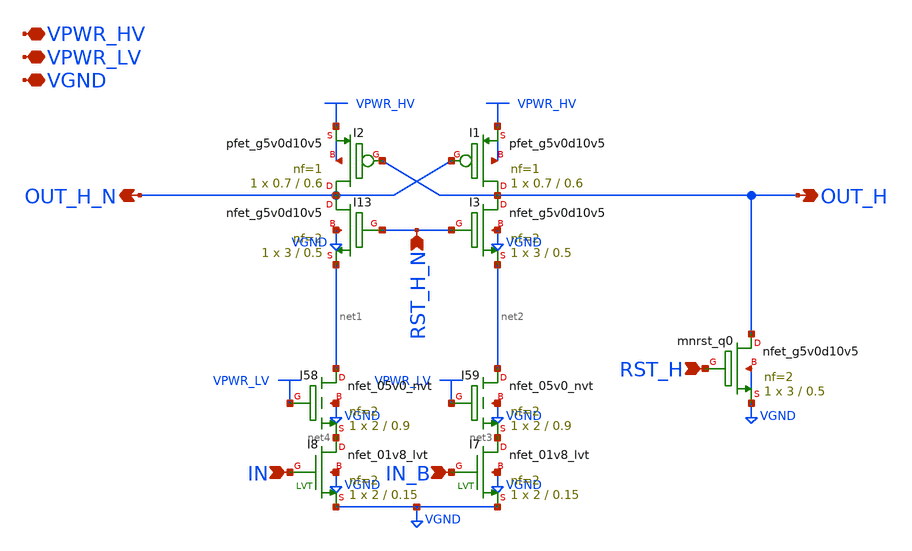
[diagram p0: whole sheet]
** sch_path: gpiov2_amux_drvr_ls.sch
* Copyright 2023 David Mitchell Bailey
* Licensed under the Apache License, Version 2.0 (the "License");
* you may not use this file except in compliance with the License.
* You may obtain a copy of the License at
* https://www.apache.org/licenses/LICENSE-2.0
* Unless required by applicable law or agreed to in writing, software
* distributed under the License is distributed on an "AS IS" BASIS,
* WITHOUT WARRANTIES OR CONDITIONS OF ANY KIND, either express or implied.
* See the License for the specific language governing permissions and
* limitations under the License.
**.subckt gpiov2_amux_drvr_ls RST_H OUT_H VPWR_LV VGND OUT_H_N RST_H_N IN IN_B VPWR_HV
*.ipin RST_H
*.opin OUT_H
*.iopin VPWR_LV
*.iopin VGND
*.opin OUT_H_N
*.ipin RST_H_N
*.ipin IN
*.ipin IN_B
*.iopin VPWR_HV
XI13 OUT_H_N RST_H_N net1 VGND sky130_fd_pr__nfet_g5v0d10v5 L=0.5 W=3 nf=2 ad='int((nf+1)/2) * W/nf * 0.29'
+ as='int((nf+2)/2) * W/nf * 0.29' pd='2*int((nf+1)/2) * (W/nf + 0.29)' ps='2*int((nf+2)/2) * (W/nf + 0.29)'
+ nrd='0.29 / W' nrs='0.29 / W' sa=0 sb=0 sd=0 mult=1 m=1
XI3 OUT_H RST_H_N net2 VGND sky130_fd_pr__nfet_g5v0d10v5 L=0.5 W=3 nf=2 ad='int((nf+1)/2) * W/nf * 0.29'
+ as='int((nf+2)/2) * W/nf * 0.29' pd='2*int((nf+1)/2) * (W/nf + 0.29)' ps='2*int((nf+2)/2) * (W/nf + 0.29)'
+ nrd='0.29 / W' nrs='0.29 / W' sa=0 sb=0 sd=0 mult=1 m=1
XI1 OUT_H OUT_H_N VPWR_HV VPWR_HV sky130_fd_pr__pfet_g5v0d10v5 L=0.6 W=0.7 nf=1 ad='int((nf+1)/2) * W/nf * 0.29'
+ as='int((nf+2)/2) * W/nf * 0.29' pd='2*int((nf+1)/2) * (W/nf + 0.29)' ps='2*int((nf+2)/2) * (W/nf + 0.29)'
+ nrd='0.29 / W' nrs='0.29 / W' sa=0 sb=0 sd=0 mult=1 m=1
XI2 OUT_H_N OUT_H VPWR_HV VPWR_HV sky130_fd_pr__pfet_g5v0d10v5 L=0.6 W=0.7 nf=1 ad='int((nf+1)/2) * W/nf * 0.29'
+ as='int((nf+2)/2) * W/nf * 0.29' pd='2*int((nf+1)/2) * (W/nf + 0.29)' ps='2*int((nf+2)/2) * (W/nf + 0.29)'
+ nrd='0.29 / W' nrs='0.29 / W' sa=0 sb=0 sd=0 mult=1 m=1
Xmnrst_q0 OUT_H RST_H VGND VGND sky130_fd_pr__nfet_g5v0d10v5 L=0.5 W=3 nf=2 ad='int((nf+1)/2) * W/nf * 0.29'
+ as='int((nf+2)/2) * W/nf * 0.29' pd='2*int((nf+1)/2) * (W/nf + 0.29)' ps='2*int((nf+2)/2) * (W/nf + 0.29)'
+ nrd='0.29 / W' nrs='0.29 / W' sa=0 sb=0 sd=0 mult=1 m=1
XI59 net2 VPWR_LV net3 VGND sky130_fd_pr__nfet_05v0_nvt L=0.9 W=2 nf=2 ad='int((nf+1)/2) * W/nf * 0.29'
+ as='int((nf+2)/2) * W/nf * 0.29' pd='2*int((nf+1)/2) * (W/nf + 0.29)' ps='2*int((nf+2)/2) * (W/nf + 0.29)'
+ nrd='0.29 / W' nrs='0.29 / W' sa=0 sb=0 sd=0 mult=1 m=1
XI58 net1 VPWR_LV net4 VGND sky130_fd_pr__nfet_05v0_nvt L=0.9 W=2 nf=2 ad='int((nf+1)/2) * W/nf * 0.29'
+ as='int((nf+2)/2) * W/nf * 0.29' pd='2*int((nf+1)/2) * (W/nf + 0.29)' ps='2*int((nf+2)/2) * (W/nf + 0.29)'
+ nrd='0.29 / W' nrs='0.29 / W' sa=0 sb=0 sd=0 mult=1 m=1
XI7 net3 IN_B VGND VGND sky130_fd_pr__nfet_01v8_lvt L=0.15 W=2 nf=2 ad='int((nf+1)/2) * W/nf * 0.29'
+ as='int((nf+2)/2) * W/nf * 0.29' pd='2*int((nf+1)/2) * (W/nf + 0.29)' ps='2*int((nf+2)/2) * (W/nf + 0.29)'
+ nrd='0.29 / W' nrs='0.29 / W' sa=0 sb=0 sd=0 mult=1 m=1
XI8 net4 IN VGND VGND sky130_fd_pr__nfet_01v8_lvt L=0.15 W=2 nf=2 ad='int((nf+1)/2) * W/nf * 0.29' as='int((nf+2)/2) * W/nf * 0.29'
+ pd='2*int((nf+1)/2) * (W/nf + 0.29)' ps='2*int((nf+2)/2) * (W/nf + 0.29)' nrd='0.29 / W' nrs='0.29 / W'
+ sa=0 sb=0 sd=0 mult=1 m=1
**.ends
.end
